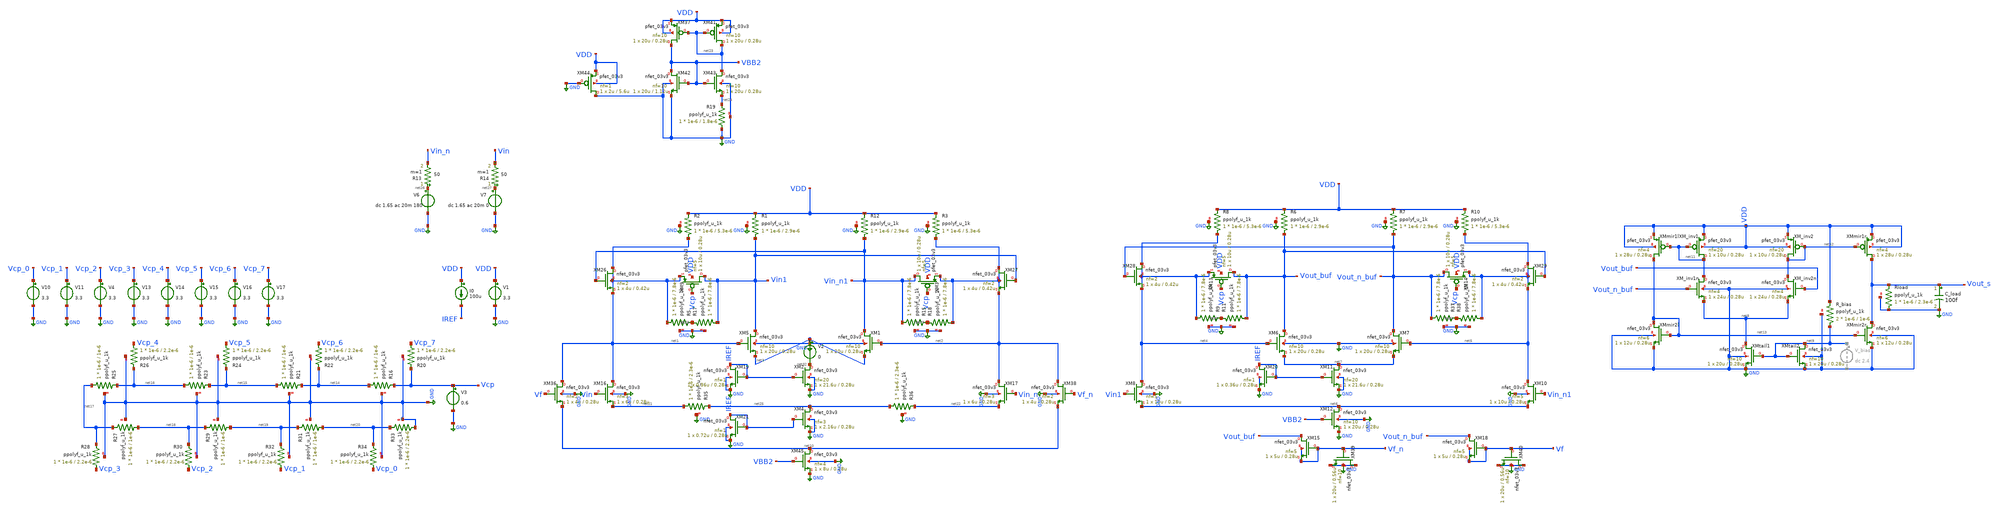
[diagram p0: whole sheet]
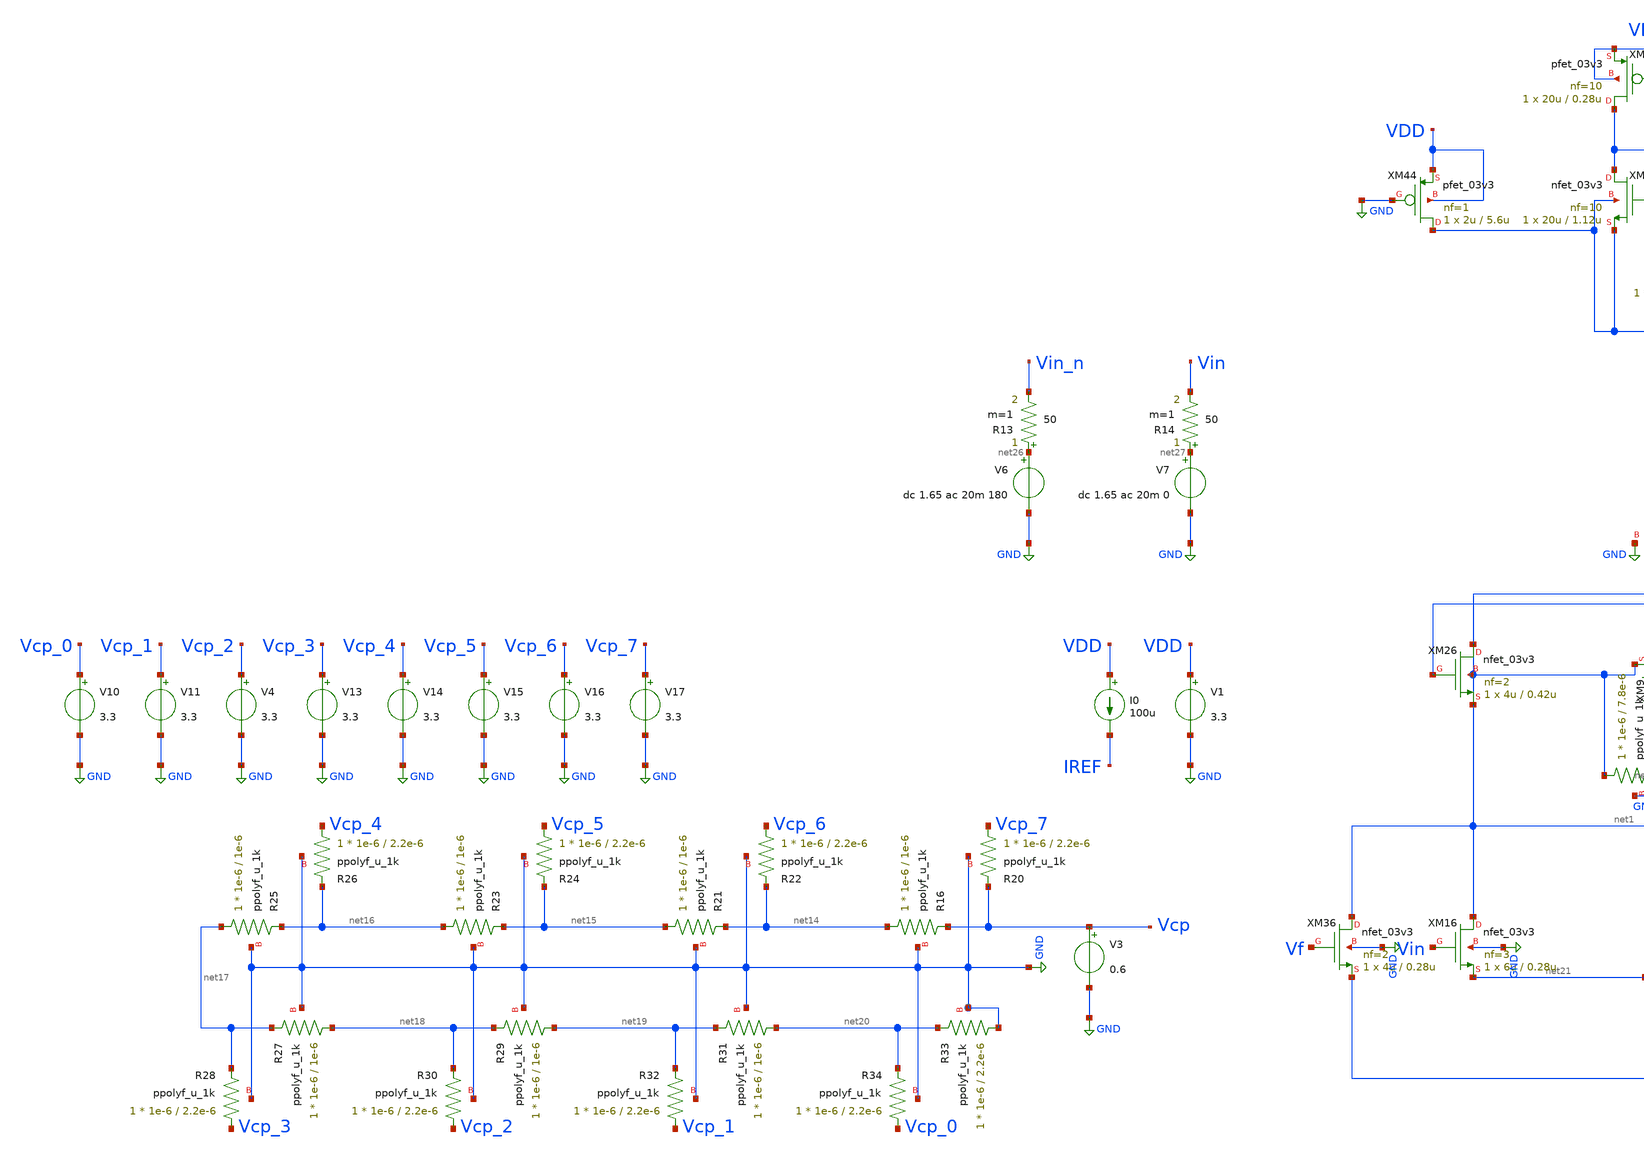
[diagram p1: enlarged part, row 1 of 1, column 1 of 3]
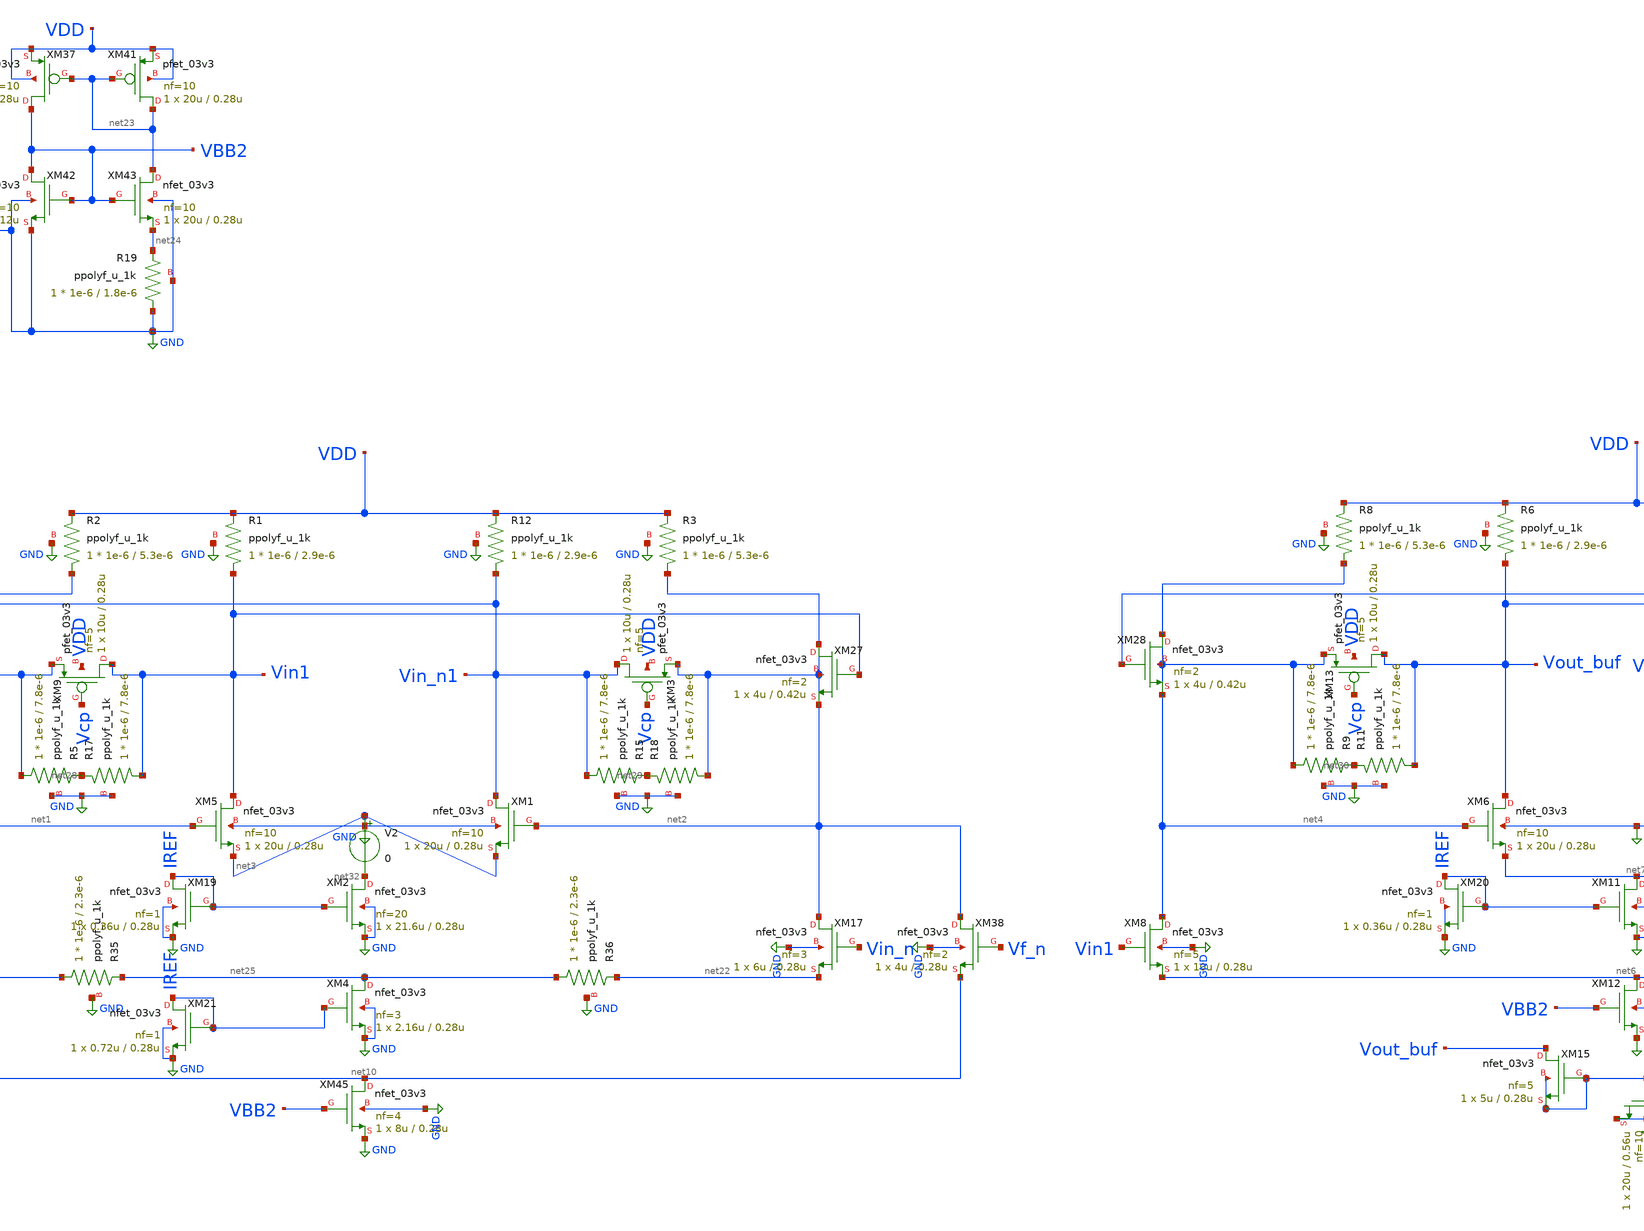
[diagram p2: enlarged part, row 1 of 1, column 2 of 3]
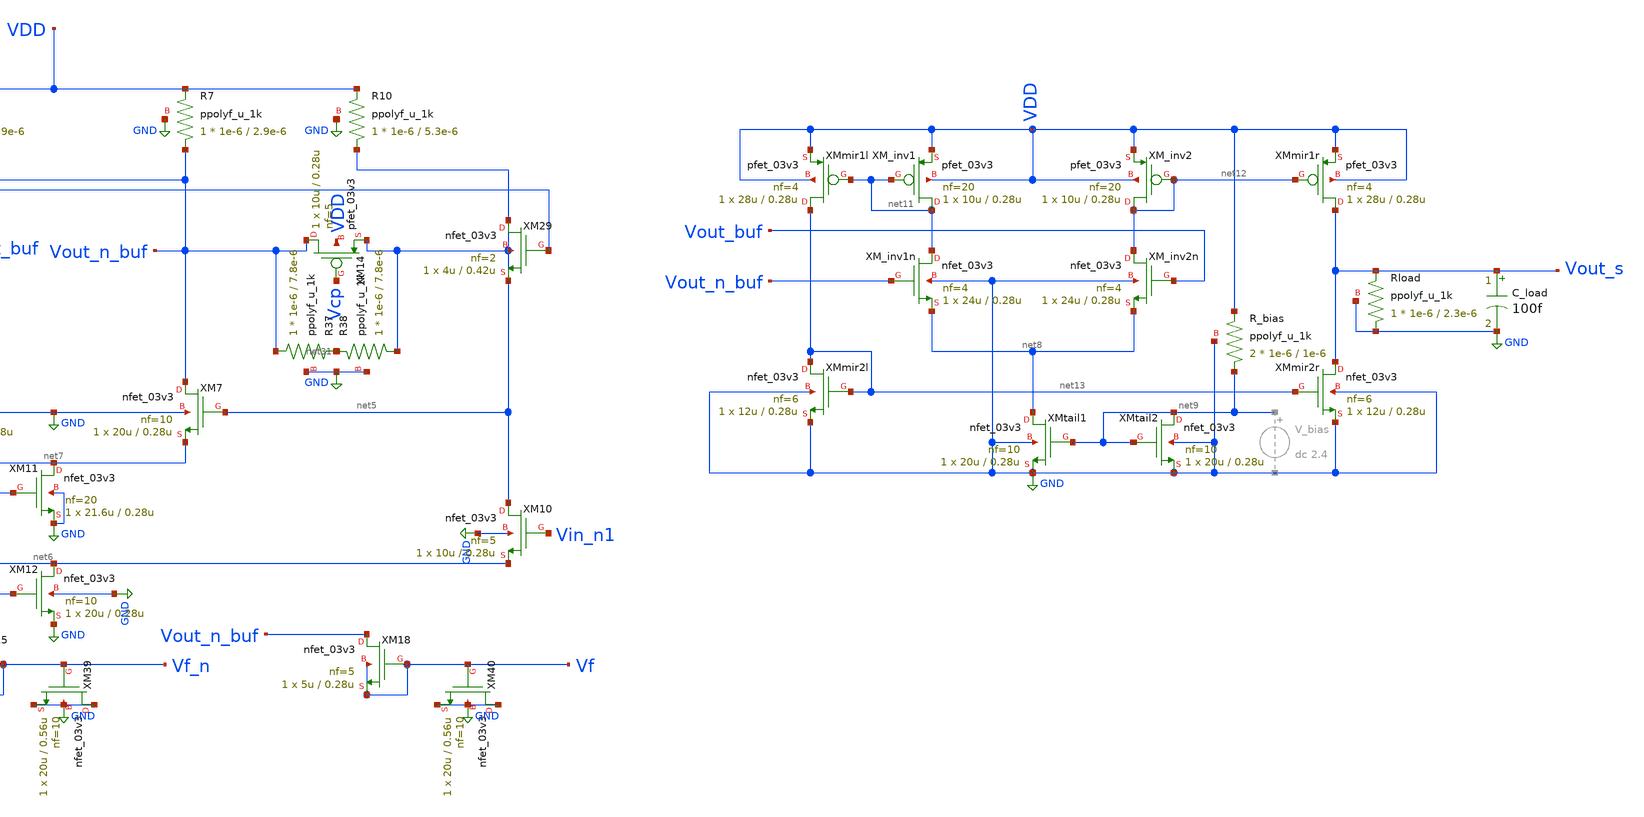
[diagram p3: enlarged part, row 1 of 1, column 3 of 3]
** sch_path: blocks/vga/vga.sch
**.subckt vga
V1 VDD GND 3.3
V6 net26 GND dc 1.65 ac 20m 180
XM5 Vin1 net1 net3 GND nfet_03v3 L=0.28u W=20u nf=10 ad='int((nf+1)/2) * W/nf * 0.18u' as='int((nf+2)/2) * W/nf * 0.18u'
+ pd='2*int((nf+1)/2) * (W/nf + 0.18u)' ps='2*int((nf+2)/2) * (W/nf + 0.18u)' nrd='0.18u / W' nrs='0.18u / W'
+ sa=0 sb=0 sd=0 m=1
XM1 Vin_n1 net2 net3 GND nfet_03v3 L=0.28u W=20u nf=10 ad='int((nf+1)/2) * W/nf * 0.18u' as='int((nf+2)/2) * W/nf * 0.18u'
+ pd='2*int((nf+1)/2) * (W/nf + 0.18u)' ps='2*int((nf+2)/2) * (W/nf + 0.18u)' nrd='0.18u / W' nrs='0.18u / W'
+ sa=0 sb=0 sd=0 m=1
XM16 net1 Vin net21 GND nfet_03v3 L=0.28u W=6u nf=3 ad='int((nf+1)/2) * W/nf * 0.18u' as='int((nf+2)/2) * W/nf * 0.18u'
+ pd='2*int((nf+1)/2) * (W/nf + 0.18u)' ps='2*int((nf+2)/2) * (W/nf + 0.18u)' nrd='0.18u / W' nrs='0.18u / W'
+ sa=0 sb=0 sd=0 m=1
XM17 net2 Vin_n net22 GND nfet_03v3 L=0.28u W=6u nf=3 ad='int((nf+1)/2) * W/nf * 0.18u' as='int((nf+2)/2) * W/nf * 0.18u'
+ pd='2*int((nf+1)/2) * (W/nf + 0.18u)' ps='2*int((nf+2)/2) * (W/nf + 0.18u)' nrd='0.18u / W' nrs='0.18u / W'
+ sa=0 sb=0 sd=0 m=1
XM9 Vin1 Vcp net1 VDD pfet_03v3 L=0.28u W=10u nf=5 ad='int((nf+1)/2) * W/nf * 0.18u' as='int((nf+2)/2) * W/nf * 0.18u'
+ pd='2*int((nf+1)/2) * (W/nf + 0.18u)' ps='2*int((nf+2)/2) * (W/nf + 0.18u)' nrd='0.18u / W' nrs='0.18u / W'
+ sa=0 sb=0 sd=0 m=1
XM6 Vout_buf net4 net7 GND nfet_03v3 L=0.28u W=20u nf=10 ad='int((nf+1)/2) * W/nf * 0.18u' as='int((nf+2)/2) * W/nf * 0.18u'
+ pd='2*int((nf+1)/2) * (W/nf + 0.18u)' ps='2*int((nf+2)/2) * (W/nf + 0.18u)' nrd='0.18u / W' nrs='0.18u / W'
+ sa=0 sb=0 sd=0 m=1
XM7 Vout_n_buf net5 net7 GND nfet_03v3 L=0.28u W=20u nf=10 ad='int((nf+1)/2) * W/nf * 0.18u' as='int((nf+2)/2) * W/nf * 0.18u'
+ pd='2*int((nf+1)/2) * (W/nf + 0.18u)' ps='2*int((nf+2)/2) * (W/nf + 0.18u)' nrd='0.18u / W' nrs='0.18u / W'
+ sa=0 sb=0 sd=0 m=1
XM8 net4 Vin1 net6 GND nfet_03v3 L=0.28u W=10u nf=5 ad='int((nf+1)/2) * W/nf * 0.18u' as='int((nf+2)/2) * W/nf * 0.18u'
+ pd='2*int((nf+1)/2) * (W/nf + 0.18u)' ps='2*int((nf+2)/2) * (W/nf + 0.18u)' nrd='0.18u / W' nrs='0.18u / W'
+ sa=0 sb=0 sd=0 m=1
XM10 net5 Vin_n1 net6 GND nfet_03v3 L=0.28u W=10u nf=5 ad='int((nf+1)/2) * W/nf * 0.18u' as='int((nf+2)/2) * W/nf * 0.18u'
+ pd='2*int((nf+1)/2) * (W/nf + 0.18u)' ps='2*int((nf+2)/2) * (W/nf + 0.18u)' nrd='0.18u / W' nrs='0.18u / W'
+ sa=0 sb=0 sd=0 m=1
XM12 net6 VBB2 GND GND nfet_03v3 L=0.28u W=20u nf=10 ad='int((nf+1)/2) * W/nf * 0.18u' as='int((nf+2)/2) * W/nf * 0.18u'
+ pd='2*int((nf+1)/2) * (W/nf + 0.18u)' ps='2*int((nf+2)/2) * (W/nf + 0.18u)' nrd='0.18u / W' nrs='0.18u / W'
+ sa=0 sb=0 sd=0 m=1
V7 net27 GND dc 1.65 ac 20m 0
R14 net27 Vin 50 m=1
R13 net26 Vin_n 50 m=1
XM26 net1 Vin_n1 net1 net1 nfet_03v3 L=0.42u W=4u nf=2 ad='int((nf+1)/2) * W/nf * 0.18u' as='int((nf+2)/2) * W/nf * 0.18u'
+ pd='2*int((nf+1)/2) * (W/nf + 0.18u)' ps='2*int((nf+2)/2) * (W/nf + 0.18u)' nrd='0.18u / W' nrs='0.18u / W'
+ sa=0 sb=0 sd=0 m=1
XM27 net2 Vin1 net2 net2 nfet_03v3 L=0.42u W=4u nf=2 ad='int((nf+1)/2) * W/nf * 0.18u' as='int((nf+2)/2) * W/nf * 0.18u'
+ pd='2*int((nf+1)/2) * (W/nf + 0.18u)' ps='2*int((nf+2)/2) * (W/nf + 0.18u)' nrd='0.18u / W' nrs='0.18u / W'
+ sa=0 sb=0 sd=0 m=1
XM28 net4 Vout_n_buf net4 net4 nfet_03v3 L=0.42u W=4u nf=2 ad='int((nf+1)/2) * W/nf * 0.18u' as='int((nf+2)/2) * W/nf * 0.18u'
+ pd='2*int((nf+1)/2) * (W/nf + 0.18u)' ps='2*int((nf+2)/2) * (W/nf + 0.18u)' nrd='0.18u / W' nrs='0.18u / W'
+ sa=0 sb=0 sd=0 m=1
XM29 net5 Vout_buf net5 net5 nfet_03v3 L=0.42u W=4u nf=2 ad='int((nf+1)/2) * W/nf * 0.18u' as='int((nf+2)/2) * W/nf * 0.18u'
+ pd='2*int((nf+1)/2) * (W/nf + 0.18u)' ps='2*int((nf+2)/2) * (W/nf + 0.18u)' nrd='0.18u / W' nrs='0.18u / W'
+ sa=0 sb=0 sd=0 m=1
XM_inv1 net11 net11 VDD VDD pfet_03v3 L=0.28u W=10u nf=20 ad='int((nf+1)/2) * W/nf * 0.18u' as='int((nf+2)/2) * W/nf * 0.18u'
+ pd='2*int((nf+1)/2) * (W/nf + 0.18u)' ps='2*int((nf+2)/2) * (W/nf + 0.18u)' nrd='0.18u / W' nrs='0.18u / W'
+ sa=0 sb=0 sd=0 m=1
XM_inv1n net11 Vout_n_buf net8 GND nfet_03v3 L=0.28u W=24u nf=4 ad='int((nf+1)/2) * W/nf * 0.18u' as='int((nf+2)/2) * W/nf * 0.18u'
+ pd='2*int((nf+1)/2) * (W/nf + 0.18u)' ps='2*int((nf+2)/2) * (W/nf + 0.18u)' nrd='0.18u / W' nrs='0.18u / W'
+ sa=0 sb=0 sd=0 m=1
XM_inv2 net12 net12 VDD VDD pfet_03v3 L=0.28u W=10u nf=20 ad='int((nf+1)/2) * W/nf * 0.18u' as='int((nf+2)/2) * W/nf * 0.18u'
+ pd='2*int((nf+1)/2) * (W/nf + 0.18u)' ps='2*int((nf+2)/2) * (W/nf + 0.18u)' nrd='0.18u / W' nrs='0.18u / W'
+ sa=0 sb=0 sd=0 m=1
XM_inv2n net12 Vout_buf net8 GND nfet_03v3 L=0.28u W=24u nf=4 ad='int((nf+1)/2) * W/nf * 0.18u' as='int((nf+2)/2) * W/nf * 0.18u'
+ pd='2*int((nf+1)/2) * (W/nf + 0.18u)' ps='2*int((nf+2)/2) * (W/nf + 0.18u)' nrd='0.18u / W' nrs='0.18u / W'
+ sa=0 sb=0 sd=0 m=1
XMtail1 net8 net9 GND GND nfet_03v3 L=0.28u W=20u nf=10 ad='int((nf+1)/2) * W/nf * 0.18u' as='int((nf+2)/2) * W/nf * 0.18u'
+ pd='2*int((nf+1)/2) * (W/nf + 0.18u)' ps='2*int((nf+2)/2) * (W/nf + 0.18u)' nrd='0.18u / W' nrs='0.18u / W'
+ sa=0 sb=0 sd=0 m=1
XMtail2 net9 net9 GND GND nfet_03v3 L=0.28u W=20u nf=10 ad='int((nf+1)/2) * W/nf * 0.18u' as='int((nf+2)/2) * W/nf * 0.18u'
+ pd='2*int((nf+1)/2) * (W/nf + 0.18u)' ps='2*int((nf+2)/2) * (W/nf + 0.18u)' nrd='0.18u / W' nrs='0.18u / W'
+ sa=0 sb=0 sd=0 m=1
XM36 net1 Vf net10 GND nfet_03v3 L=0.28u W=4u nf=2 ad='int((nf+1)/2) * W/nf * 0.18u' as='int((nf+2)/2) * W/nf * 0.18u'
+ pd='2*int((nf+1)/2) * (W/nf + 0.18u)' ps='2*int((nf+2)/2) * (W/nf + 0.18u)' nrd='0.18u / W' nrs='0.18u / W'
+ sa=0 sb=0 sd=0 m=1
XM38 net2 Vf_n net10 GND nfet_03v3 L=0.28u W=4u nf=2 ad='int((nf+1)/2) * W/nf * 0.18u' as='int((nf+2)/2) * W/nf * 0.18u'
+ pd='2*int((nf+1)/2) * (W/nf + 0.18u)' ps='2*int((nf+2)/2) * (W/nf + 0.18u)' nrd='0.18u / W' nrs='0.18u / W'
+ sa=0 sb=0 sd=0 m=1
XM39 GND Vf_n GND GND nfet_03v3 L=0.56u W=20u nf=10 ad='int((nf+1)/2) * W/nf * 0.18u' as='int((nf+2)/2) * W/nf * 0.18u'
+ pd='2*int((nf+1)/2) * (W/nf + 0.18u)' ps='2*int((nf+2)/2) * (W/nf + 0.18u)' nrd='0.18u / W' nrs='0.18u / W'
+ sa=0 sb=0 sd=0 m=1
XM40 GND Vf GND GND nfet_03v3 L=0.56u W=20u nf=10 ad='int((nf+1)/2) * W/nf * 0.18u' as='int((nf+2)/2) * W/nf * 0.18u'
+ pd='2*int((nf+1)/2) * (W/nf + 0.18u)' ps='2*int((nf+2)/2) * (W/nf + 0.18u)' nrd='0.18u / W' nrs='0.18u / W'
+ sa=0 sb=0 sd=0 m=1
XM45 net10 VBB2 GND GND nfet_03v3 L=0.28u W=8u nf=4 ad='int((nf+1)/2) * W/nf * 0.18u' as='int((nf+2)/2) * W/nf * 0.18u'
+ pd='2*int((nf+1)/2) * (W/nf + 0.18u)' ps='2*int((nf+2)/2) * (W/nf + 0.18u)' nrd='0.18u / W' nrs='0.18u / W'
+ sa=0 sb=0 sd=0 m=1
XMmir1l net13 net11 VDD VDD pfet_03v3 L=0.28u W=28u nf=4 ad='int((nf+1)/2) * W/nf * 0.18u' as='int((nf+2)/2) * W/nf * 0.18u'
+ pd='2*int((nf+1)/2) * (W/nf + 0.18u)' ps='2*int((nf+2)/2) * (W/nf + 0.18u)' nrd='0.18u / W' nrs='0.18u / W'
+ sa=0 sb=0 sd=0 m=1
XMmir1r Vout_s net12 VDD VDD pfet_03v3 L=0.28u W=28u nf=4 ad='int((nf+1)/2) * W/nf * 0.18u' as='int((nf+2)/2) * W/nf * 0.18u'
+ pd='2*int((nf+1)/2) * (W/nf + 0.18u)' ps='2*int((nf+2)/2) * (W/nf + 0.18u)' nrd='0.18u / W' nrs='0.18u / W'
+ sa=0 sb=0 sd=0 m=1
XMmir2l net13 net13 GND GND nfet_03v3 L=0.28u W=12u nf=6 ad='int((nf+1)/2) * W/nf * 0.18u' as='int((nf+2)/2) * W/nf * 0.18u'
+ pd='2*int((nf+1)/2) * (W/nf + 0.18u)' ps='2*int((nf+2)/2) * (W/nf + 0.18u)' nrd='0.18u / W' nrs='0.18u / W'
+ sa=0 sb=0 sd=0 m=1
XMmir2r Vout_s net13 GND GND nfet_03v3 L=0.28u W=12u nf=6 ad='int((nf+1)/2) * W/nf * 0.18u' as='int((nf+2)/2) * W/nf * 0.18u'
+ pd='2*int((nf+1)/2) * (W/nf + 0.18u)' ps='2*int((nf+2)/2) * (W/nf + 0.18u)' nrd='0.18u / W' nrs='0.18u / W'
+ sa=0 sb=0 sd=0 m=1
XR_bias net9 VDD GND ppolyf_u_1k r_width=1e-6 r_length=1e-6 m=2
C_load Vout_s GND 100f m=1
XR16 net14 Vcp GND ppolyf_u_1k r_width=1e-6 r_length=1e-6 m=1
XR20 Vcp_7 Vcp GND ppolyf_u_1k r_width=1e-6 r_length=2.2e-6 m=1
XR21 net15 net14 GND ppolyf_u_1k r_width=1e-6 r_length=1e-6 m=1
XR22 Vcp_6 net14 GND ppolyf_u_1k r_width=1e-6 r_length=2.2e-6 m=1
XR23 net16 net15 GND ppolyf_u_1k r_width=1e-6 r_length=1e-6 m=1
XR24 Vcp_5 net15 GND ppolyf_u_1k r_width=1e-6 r_length=2.2e-6 m=1
XR25 net17 net16 GND ppolyf_u_1k r_width=1e-6 r_length=1e-6 m=1
XR26 Vcp_4 net16 GND ppolyf_u_1k r_width=1e-6 r_length=2.2e-6 m=1
XR27 net18 net17 GND ppolyf_u_1k r_width=1e-6 r_length=1e-6 m=1
XR28 Vcp_3 net17 GND ppolyf_u_1k r_width=1e-6 r_length=2.2e-6 m=1
XR29 net19 net18 GND ppolyf_u_1k r_width=1e-6 r_length=1e-6 m=1
XR30 Vcp_2 net18 GND ppolyf_u_1k r_width=1e-6 r_length=2.2e-6 m=1
XR31 net20 net19 GND ppolyf_u_1k r_width=1e-6 r_length=1e-6 m=1
XR32 Vcp_1 net19 GND ppolyf_u_1k r_width=1e-6 r_length=2.2e-6 m=1
XR33 GND net20 GND ppolyf_u_1k r_width=1e-6 r_length=2.2e-6 m=1
XR34 Vcp_0 net20 GND ppolyf_u_1k r_width=1e-6 r_length=2.2e-6 m=1
V10 Vcp_0 GND 3.3
V11 Vcp_1 GND 3.3
V4 Vcp_2 GND 3.3
V13 Vcp_3 GND 3.3
V14 Vcp_4 GND 3.3
V15 Vcp_5 GND 3.3
V16 Vcp_6 GND 3.3
V17 Vcp_7 GND 3.3
V3 Vcp GND 0.6
XR35 net21 net25 GND ppolyf_u_1k r_width=1e-6 r_length=2.3e-6 m=1
XR36 net25 net22 GND ppolyf_u_1k r_width=1e-6 r_length=2.3e-6 m=1
XM15 Vout_buf Vf_n Vf_n Vf_n nfet_03v3 L=0.28u W=5u nf=5 ad='int((nf+1)/2) * W/nf * 0.18u' as='int((nf+2)/2) * W/nf * 0.18u'
+ pd='2*int((nf+1)/2) * (W/nf + 0.18u)' ps='2*int((nf+2)/2) * (W/nf + 0.18u)' nrd='0.18u / W' nrs='0.18u / W'
+ sa=0 sb=0 sd=0 m=1
XM18 Vout_n_buf Vf Vf Vf nfet_03v3 L=0.28u W=5u nf=5 ad='int((nf+1)/2) * W/nf * 0.18u' as='int((nf+2)/2) * W/nf * 0.18u'
+ pd='2*int((nf+1)/2) * (W/nf + 0.18u)' ps='2*int((nf+2)/2) * (W/nf + 0.18u)' nrd='0.18u / W' nrs='0.18u / W'
+ sa=0 sb=0 sd=0 m=1
XR5 net1 net28 GND ppolyf_u_1k r_width=1e-6 r_length=7.8e-6 m=1
XR17 Vin1 net28 GND ppolyf_u_1k r_width=1e-6 r_length=7.8e-6 m=1
XM3 Vin_n1 Vcp net2 VDD pfet_03v3 L=0.28u W=10u nf=5 ad='int((nf+1)/2) * W/nf * 0.18u' as='int((nf+2)/2) * W/nf * 0.18u'
+ pd='2*int((nf+1)/2) * (W/nf + 0.18u)' ps='2*int((nf+2)/2) * (W/nf + 0.18u)' nrd='0.18u / W' nrs='0.18u / W'
+ sa=0 sb=0 sd=0 m=1
XR15 Vin_n1 net29 GND ppolyf_u_1k r_width=1e-6 r_length=7.8e-6 m=1
XR18 net2 net29 GND ppolyf_u_1k r_width=1e-6 r_length=7.8e-6 m=1
XM13 Vout_buf Vcp net4 VDD pfet_03v3 L=0.28u W=10u nf=5 ad='int((nf+1)/2) * W/nf * 0.18u' as='int((nf+2)/2) * W/nf * 0.18u'
+ pd='2*int((nf+1)/2) * (W/nf + 0.18u)' ps='2*int((nf+2)/2) * (W/nf + 0.18u)' nrd='0.18u / W' nrs='0.18u / W'
+ sa=0 sb=0 sd=0 m=1
XR9 net4 net30 GND ppolyf_u_1k r_width=1e-6 r_length=7.8e-6 m=1
XR11 Vout_buf net30 GND ppolyf_u_1k r_width=1e-6 r_length=7.8e-6 m=1
XM14 Vout_n_buf Vcp net5 VDD pfet_03v3 L=0.28u W=10u nf=5 ad='int((nf+1)/2) * W/nf * 0.18u' as='int((nf+2)/2) * W/nf * 0.18u'
+ pd='2*int((nf+1)/2) * (W/nf + 0.18u)' ps='2*int((nf+2)/2) * (W/nf + 0.18u)' nrd='0.18u / W' nrs='0.18u / W'
+ sa=0 sb=0 sd=0 m=1
XR37 Vout_n_buf net31 GND ppolyf_u_1k r_width=1e-6 r_length=7.8e-6 m=1
XR38 net5 net31 GND ppolyf_u_1k r_width=1e-6 r_length=7.8e-6 m=1
XRload GND Vout_s GND ppolyf_u_1k r_width=1e-6 r_length=2.3e-6 m=1
XR1 Vin1 VDD GND ppolyf_u_1k r_width=1e-6 r_length=2.9e-6 m=1
XR12 Vin_n1 VDD GND ppolyf_u_1k r_width=1e-6 r_length=2.9e-6 m=1
XR6 Vout_buf VDD GND ppolyf_u_1k r_width=1e-6 r_length=2.9e-6 m=1
XR7 Vout_n_buf VDD GND ppolyf_u_1k r_width=1e-6 r_length=2.9e-6 m=1
XR3 net2 VDD GND ppolyf_u_1k r_width=1e-6 r_length=5.3e-6 m=1
XR2 net1 VDD GND ppolyf_u_1k r_width=1e-6 r_length=5.3e-6 m=1
XR8 net4 VDD GND ppolyf_u_1k r_width=1e-6 r_length=5.3e-6 m=1
XR10 net5 VDD GND ppolyf_u_1k r_width=1e-6 r_length=5.3e-6 m=1
I0 VDD IREF 100u
XM2 net32 IREF GND GND nfet_03v3 L=0.28u W=21.6u nf=20 ad='int((nf+1)/2) * W/nf * 0.18u' as='int((nf+2)/2) * W/nf * 0.18u'
+ pd='2*int((nf+1)/2) * (W/nf + 0.18u)' ps='2*int((nf+2)/2) * (W/nf + 0.18u)' nrd='0.18u / W' nrs='0.18u / W'
+ sa=0 sb=0 sd=0 m=1
XM19 IREF IREF GND GND nfet_03v3 L=0.28u W=0.36u nf=1 ad='int((nf+1)/2) * W/nf * 0.18u' as='int((nf+2)/2) * W/nf * 0.18u'
+ pd='2*int((nf+1)/2) * (W/nf + 0.18u)' ps='2*int((nf+2)/2) * (W/nf + 0.18u)' nrd='0.18u / W' nrs='0.18u / W'
+ sa=0 sb=0 sd=0 m=1
XM11 net7 IREF GND GND nfet_03v3 L=0.28u W=21.6u nf=20 ad='int((nf+1)/2) * W/nf * 0.18u' as='int((nf+2)/2) * W/nf * 0.18u'
+ pd='2*int((nf+1)/2) * (W/nf + 0.18u)' ps='2*int((nf+2)/2) * (W/nf + 0.18u)' nrd='0.18u / W' nrs='0.18u / W'
+ sa=0 sb=0 sd=0 m=1
XM20 IREF IREF GND GND nfet_03v3 L=0.28u W=0.36u nf=1 ad='int((nf+1)/2) * W/nf * 0.18u' as='int((nf+2)/2) * W/nf * 0.18u'
+ pd='2*int((nf+1)/2) * (W/nf + 0.18u)' ps='2*int((nf+2)/2) * (W/nf + 0.18u)' nrd='0.18u / W' nrs='0.18u / W'
+ sa=0 sb=0 sd=0 m=1
XM37 VBB2 net23 VDD VDD pfet_03v3 L=0.28u W=20u nf=10 ad='int((nf+1)/2) * W/nf * 0.18u' as='int((nf+2)/2) * W/nf * 0.18u'
+ pd='2*int((nf+1)/2) * (W/nf + 0.18u)' ps='2*int((nf+2)/2) * (W/nf + 0.18u)' nrd='0.18u / W' nrs='0.18u / W'
+ sa=0 sb=0 sd=0 m=1
XM41 net23 net23 VDD VDD pfet_03v3 L=0.28u W=20u nf=10 ad='int((nf+1)/2) * W/nf * 0.18u' as='int((nf+2)/2) * W/nf * 0.18u'
+ pd='2*int((nf+1)/2) * (W/nf + 0.18u)' ps='2*int((nf+2)/2) * (W/nf + 0.18u)' nrd='0.18u / W' nrs='0.18u / W'
+ sa=0 sb=0 sd=0 m=1
XM42 VBB2 VBB2 GND GND nfet_03v3 L=1.12u W=20u nf=10 ad='int((nf+1)/2) * W/nf * 0.18u' as='int((nf+2)/2) * W/nf * 0.18u'
+ pd='2*int((nf+1)/2) * (W/nf + 0.18u)' ps='2*int((nf+2)/2) * (W/nf + 0.18u)' nrd='0.18u / W' nrs='0.18u / W'
+ sa=0 sb=0 sd=0 m=1
XM43 net23 VBB2 net24 GND nfet_03v3 L=0.28u W=20u nf=10 ad='int((nf+1)/2) * W/nf * 0.18u' as='int((nf+2)/2) * W/nf * 0.18u'
+ pd='2*int((nf+1)/2) * (W/nf + 0.18u)' ps='2*int((nf+2)/2) * (W/nf + 0.18u)' nrd='0.18u / W' nrs='0.18u / W'
+ sa=0 sb=0 sd=0 m=1
XM44 GND GND VDD VDD pfet_03v3 L=5.6u W=2u nf=1 ad='int((nf+1)/2) * W/nf * 0.18u' as='int((nf+2)/2) * W/nf * 0.18u'
+ pd='2*int((nf+1)/2) * (W/nf + 0.18u)' ps='2*int((nf+2)/2) * (W/nf + 0.18u)' nrd='0.18u / W' nrs='0.18u / W'
+ sa=0 sb=0 sd=0 m=1
XR19 GND net24 GND ppolyf_u_1k r_width=1e-6 r_length=1.8e-6 m=1
V2 net3 net32 0
XM4 net25 IREF GND GND nfet_03v3 L=0.28u W=2.16u nf=3 ad='int((nf+1)/2) * W/nf * 0.18u' as='int((nf+2)/2) * W/nf * 0.18u'
+ pd='2*int((nf+1)/2) * (W/nf + 0.18u)' ps='2*int((nf+2)/2) * (W/nf + 0.18u)' nrd='0.18u / W' nrs='0.18u / W'
+ sa=0 sb=0 sd=0 m=1
XM21 IREF IREF GND GND nfet_03v3 L=0.28u W=0.72u nf=1 ad='int((nf+1)/2) * W/nf * 0.18u' as='int((nf+2)/2) * W/nf * 0.18u'
+ pd='2*int((nf+1)/2) * (W/nf + 0.18u)' ps='2*int((nf+2)/2) * (W/nf + 0.18u)' nrd='0.18u / W' nrs='0.18u / W'
+ sa=0 sb=0 sd=0 m=1
**** begin user architecture code


.include /foss/pdks/gf180mcuD/libs.tech/ngspice/design.ngspice
.lib /foss/pdks/gf180mcuD/libs.tech/ngspice/sm141064.ngspice typical
.lib /foss/pdks/gf180mcuD/libs.tech/ngspice/sm141064.ngspice bjt_typical
.lib /foss/pdks/gf180mcuD/libs.tech/ngspice/sm141064.ngspice diode_typical
.lib /foss/pdks/gf180mcuD/libs.tech/ngspice/sm141064.ngspice res_typical
.lib /foss/pdks/gf180mcuD/libs.tech/ngspice/sm141064.ngspice mimcap_typical
.lib /foss/pdks/gf180mcuD/libs.tech/ngspice/sm141064.ngspice moscap_typical
.option method=gear

.control
set temp = 85
  * 1. Setup the sweep parameters
  let v_ctrl = 0.6

  let f_start = 1
  let f_stop = 3.2G
  let f_points = 120

  * 2. Initialize vectors to store results
  let gain_db = unitvec(f_points)

  alter v3 = v_ctrl
  ac dec $&f_points $&f_start $&f_stop

  * 4. Calculate Differential Gain in dB
  * Formula: 20 * log10(|Vout_diff| / |Vin_diff|)
  let vin_mag = mag(v(vin) - v(vin_n))
  let vout_s_mag = mag(v(vout_s))
  let vout_buf_mag = mag(v(vout_buf) - v(vout_n_buf))
  let vout_s_gain = 20 * log10(vout_s_mag / vin_mag)
  let vout_buf_gain = 20 * log10(vout_buf_mag / vin_mag)

  * Credit to marcel hendrix
  * https://sourceforge.net/p/ngspice/discussion/133842/thread/2031ad61/
  meas ac peak  MAX  vmag(vout_s) FROM=$&f_start TO=$&f_stop
  let f3db = peak/sqrt(2)
  meas ac lo_3db WHEN vmag(vout_s)=f3db RISE=1
  meas ac hi_3db WHEN vmag(vout_s)=f3db FALL=1

  * 5. Save results to vectors
  plot vout_s_gain vout_buf_gain title 'Gain (dB) vs. Frequency from 1MHz to 3.2GHz, 0.6 vctrl' ylimit
+ 0 80
.endc


**** end user architecture code
**.ends
.GLOBAL GND
.end
